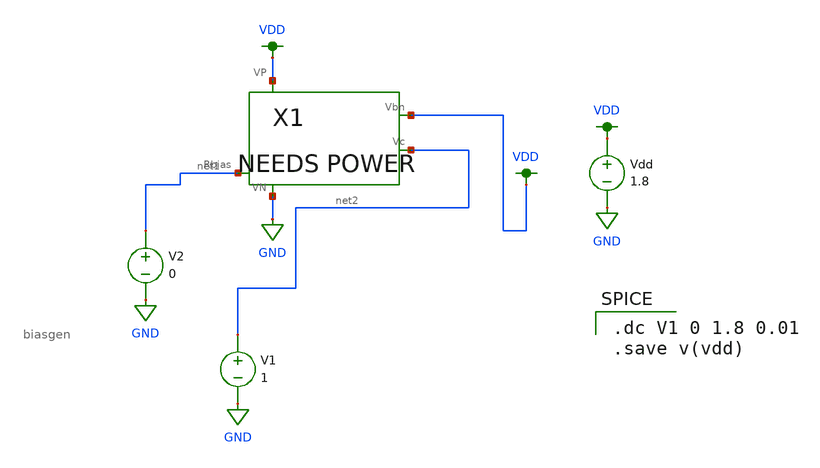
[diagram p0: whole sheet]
** sch_path: design-files/untitled.sch
**.subckt untitled
V1 net2 GND 1
V2 net1 GND 0
Vdd VDD GND 1.8
X1 net1 VDD net2 VDD GND biasgen
**** begin user architecture code

.option wnflag=1
.param MC_SWITCH=0.0
.lib ~/skywater/skywater-pdk/libraries/sky130_fd_pr_ngspice/latest/models/sky130.lib.spice tt


.dc V1 0 1.8 0.01
.save v(vdd)

**** end user architecture code
**.ends
.GLOBAL VDD
.GLOBAL GND
.end
